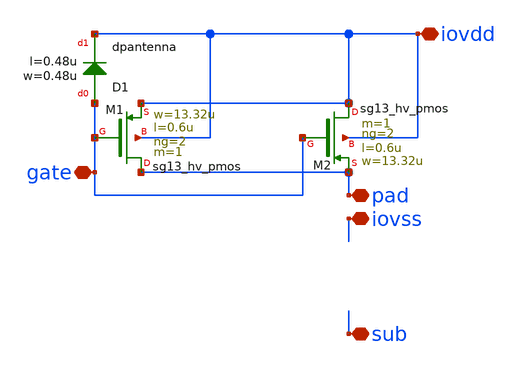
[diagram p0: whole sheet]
** sch_path: MSPHY6034-main/schematic/xschem/openpdk-libraries/ihp-sg13g2/sg13g2_io/xschem/sg13g2_Clamp_P2N2D_noptap.sch
**.subckt sg13g2_Clamp_P2N2D_noptap iovss gate pad iovdd sub
*.iopin iovss
*.iopin gate
*.iopin pad
*.iopin iovdd
*.iopin sub
XM1 pad gate iovdd iovdd sg13_hv_pmos w=13.32u l=0.6u ng=2 m=1 mm_ok=1
XM2 iovdd gate pad iovdd sg13_hv_pmos w=13.32u l=0.6u ng=2 m=1 mm_ok=1
XD1 gate iovdd dpantenna l=0.48u w=0.48u
**.ends
.end
